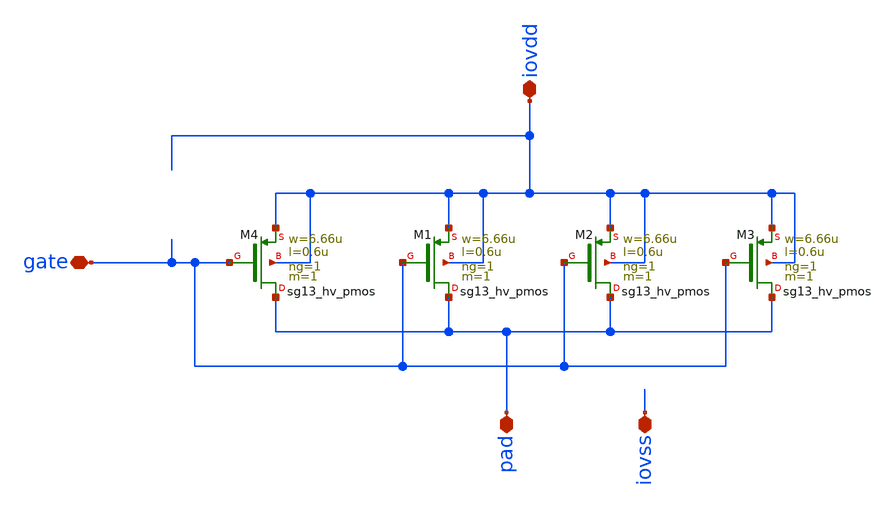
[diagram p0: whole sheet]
** sch_path: ihp-sg13g2/libs.ref/sg13g2_io/xschem/sg13g2_Clamp_P2N2D.sch
**.subckt sg13g2_Clamp_P2N2D pad iovdd gate iovss
*.iopin pad
*.iopin iovdd
*.iopin gate
*.iopin iovss
XM1 pad gate iovdd iovdd sg13_hv_pmos w=6.66u l=0.6u ng=1 m=1
XM2 pad gate iovdd iovdd sg13_hv_pmos w=6.66u l=0.6u ng=1 m=1
XM3 pad gate iovdd iovdd sg13_hv_pmos w=6.66u l=0.6u ng=1 m=1
XM4 pad gate iovdd iovdd sg13_hv_pmos w=6.66u l=0.6u ng=1 m=1
**.ends
.end
